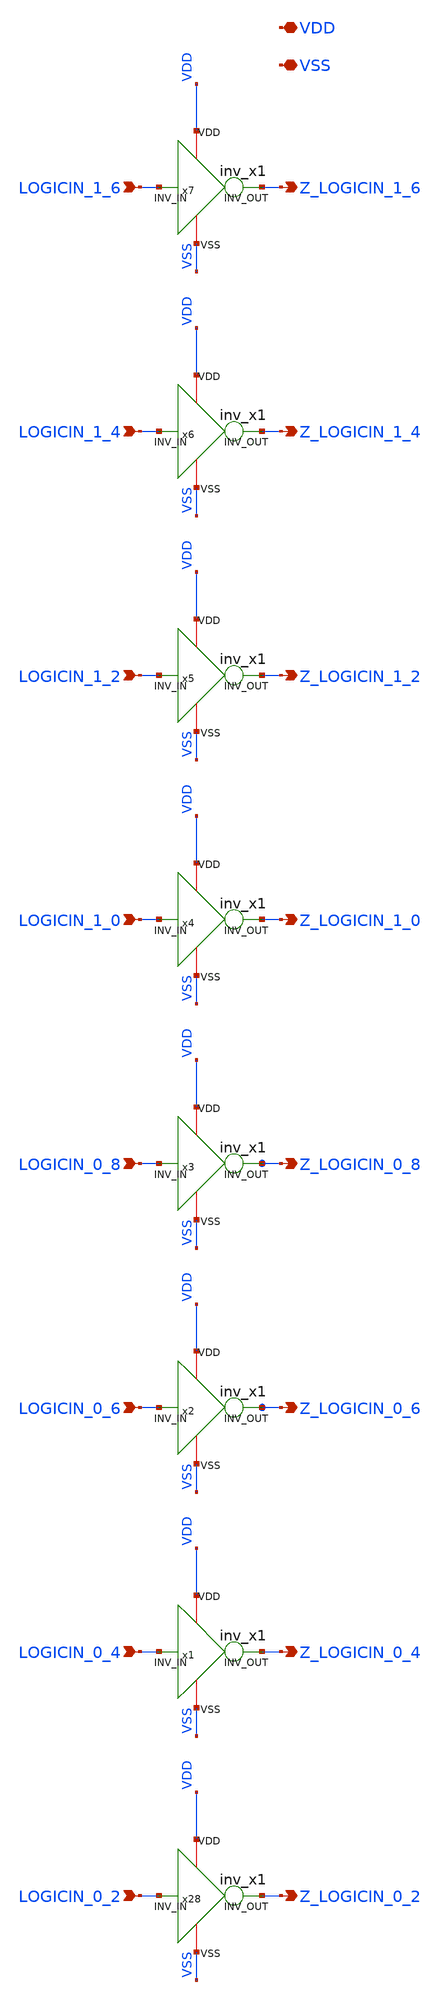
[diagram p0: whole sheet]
** sch_path: xschem/LOGIC_INV.sch
**.subckt LOGIC_INV Z_LOGICIN_0_2 LOGICIN_0_2 LOGICIN_0_4 LOGICIN_0_6 LOGICIN_0_8 LOGICIN_1_0
*+ LOGICIN_1_2 LOGICIN_1_4 LOGICIN_1_6 Z_LOGICIN_0_4 Z_LOGICIN_0_6 Z_LOGICIN_0_8 Z_LOGICIN_1_0 Z_LOGICIN_1_2
*+ Z_LOGICIN_1_4 Z_LOGICIN_1_6 VDD VSS
*.opin Z_LOGICIN_0_2
*.ipin LOGICIN_0_2
*.ipin LOGICIN_0_4
*.ipin LOGICIN_0_6
*.ipin LOGICIN_0_8
*.ipin LOGICIN_1_0
*.ipin LOGICIN_1_2
*.ipin LOGICIN_1_4
*.ipin LOGICIN_1_6
*.opin Z_LOGICIN_0_4
*.opin Z_LOGICIN_0_6
*.opin Z_LOGICIN_0_8
*.opin Z_LOGICIN_1_0
*.opin Z_LOGICIN_1_2
*.opin Z_LOGICIN_1_4
*.opin Z_LOGICIN_1_6
*.iopin VDD
*.iopin VSS
x28 VDD VSS Z_LOGICIN_0_2 LOGICIN_0_2 inv_x1
x1 VDD VSS Z_LOGICIN_0_4 LOGICIN_0_4 inv_x1
x2 VDD VSS Z_LOGICIN_0_6 LOGICIN_0_6 inv_x1
x3 VDD VSS Z_LOGICIN_0_8 LOGICIN_0_8 inv_x1
x4 VDD VSS Z_LOGICIN_1_0 LOGICIN_1_0 inv_x1
x5 VDD VSS Z_LOGICIN_1_2 LOGICIN_1_2 inv_x1
x6 VDD VSS Z_LOGICIN_1_4 LOGICIN_1_4 inv_x1
x7 VDD VSS Z_LOGICIN_1_6 LOGICIN_1_6 inv_x1
**.ends

* expanding   symbol:  inv_x1.sym # of pins=4
** sym_path: xschem/inv_x1.sym
** sch_path: xschem/inv_x1.sch
.subckt inv_x1 VDD VSS INV_OUT INV_IN
*.ipin INV_IN
*.opin INV_OUT
*.iopin VDD
*.iopin VSS
XM3 INV_OUT INV_IN VDD VDD sky130_fd_pr__pfet_01v8 L=0.15 W=1 nf=1 ad='int((nf+1)/2) * W/nf * 0.29' as='int((nf+2)/2) * W/nf * 0.29'
+ pd='2*int((nf+1)/2) * (W/nf + 0.29)' ps='2*int((nf+2)/2) * (W/nf + 0.29)' nrd='0.29 / W' nrs='0.29 / W'
+ sa=0 sb=0 sd=0 mult=1 m=1
XM5 INV_OUT INV_IN VSS VSS sky130_fd_pr__nfet_01v8 L=0.15 W=1 nf=1 ad='int((nf+1)/2) * W/nf * 0.29' as='int((nf+2)/2) * W/nf * 0.29'
+ pd='2*int((nf+1)/2) * (W/nf + 0.29)' ps='2*int((nf+2)/2) * (W/nf + 0.29)' nrd='0.29 / W' nrs='0.29 / W'
+ sa=0 sb=0 sd=0 mult=1 m=1
.ends

.end
